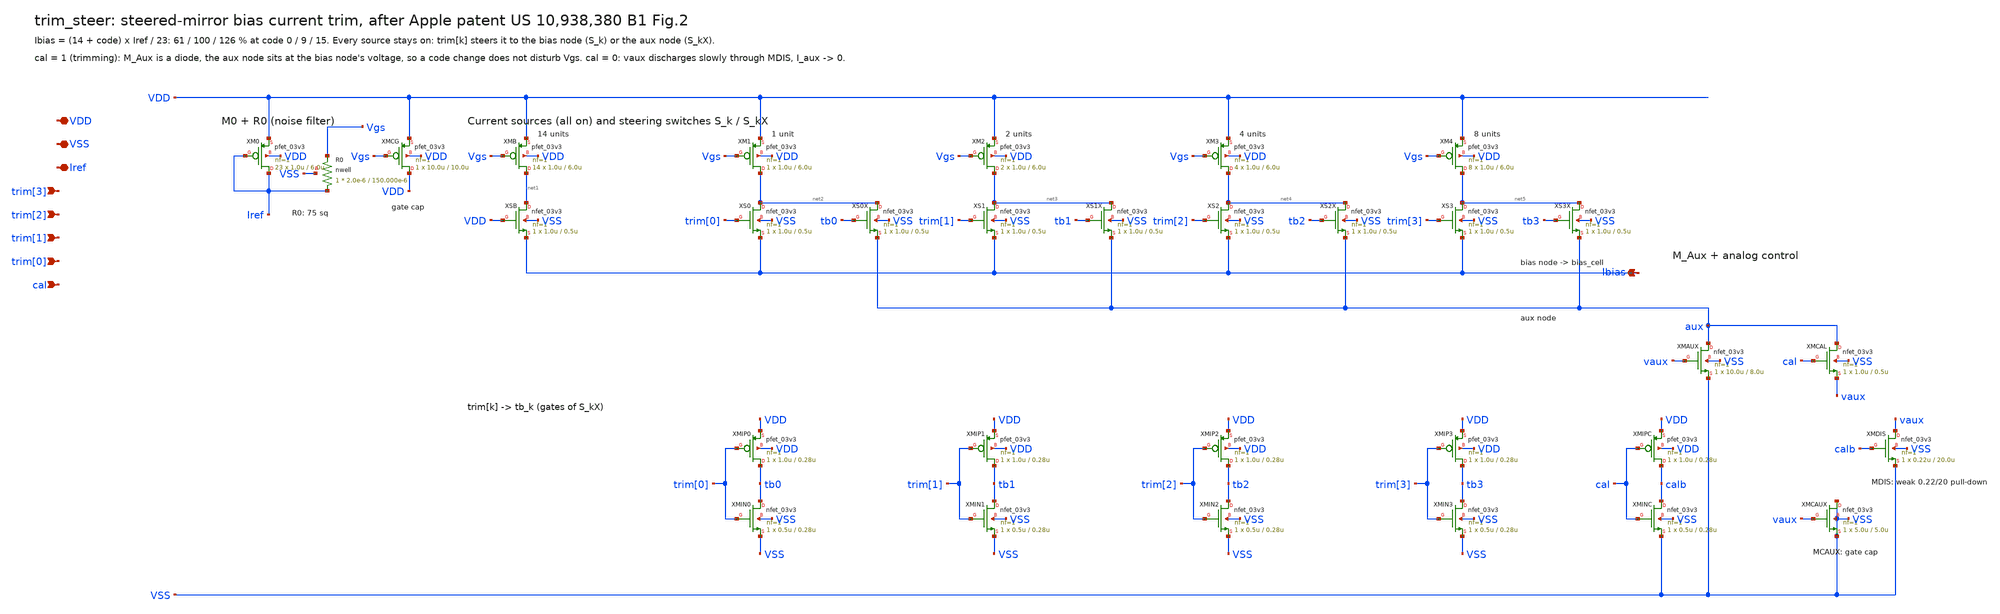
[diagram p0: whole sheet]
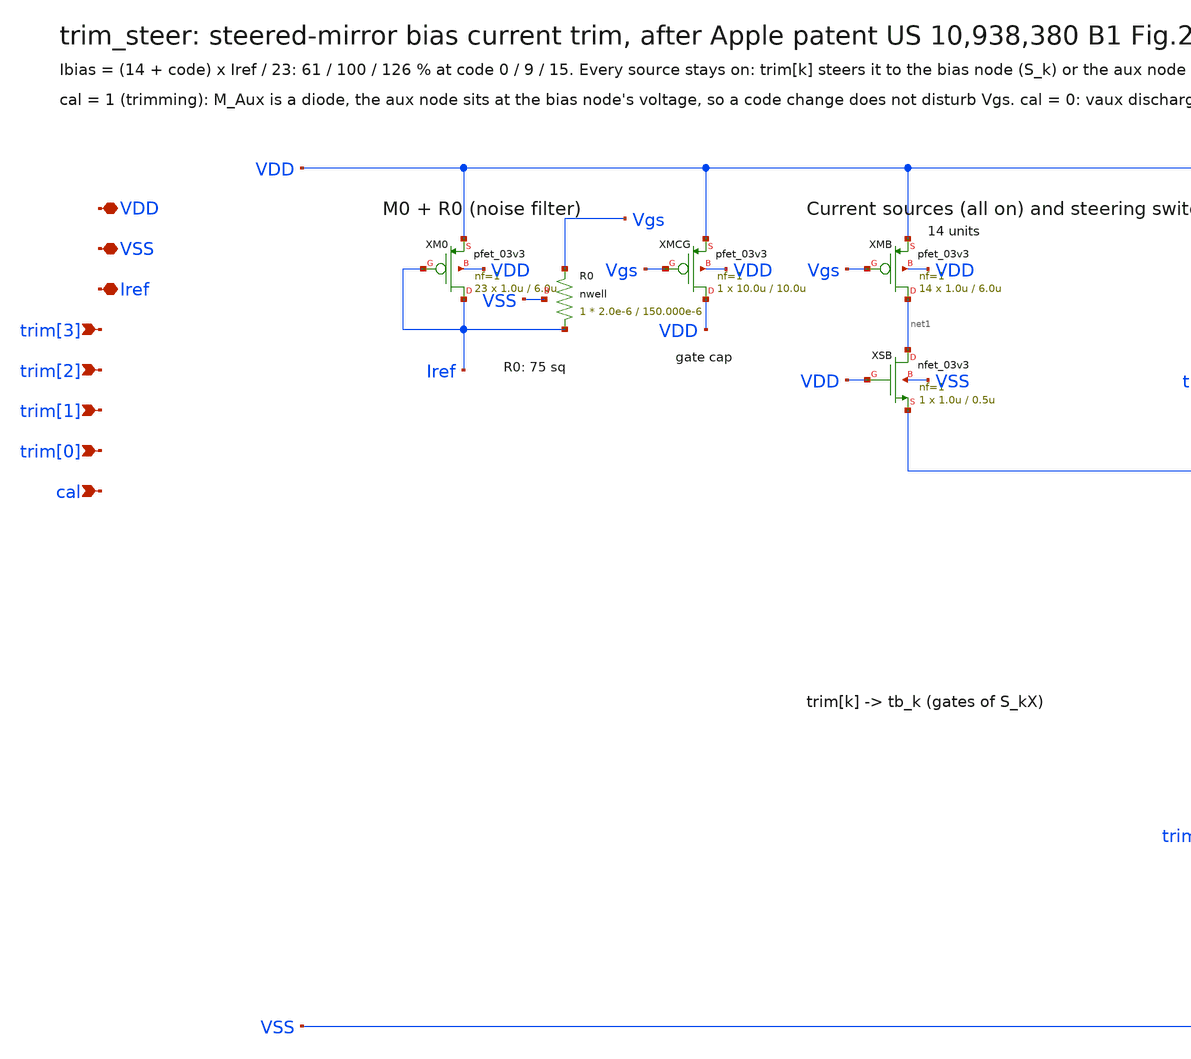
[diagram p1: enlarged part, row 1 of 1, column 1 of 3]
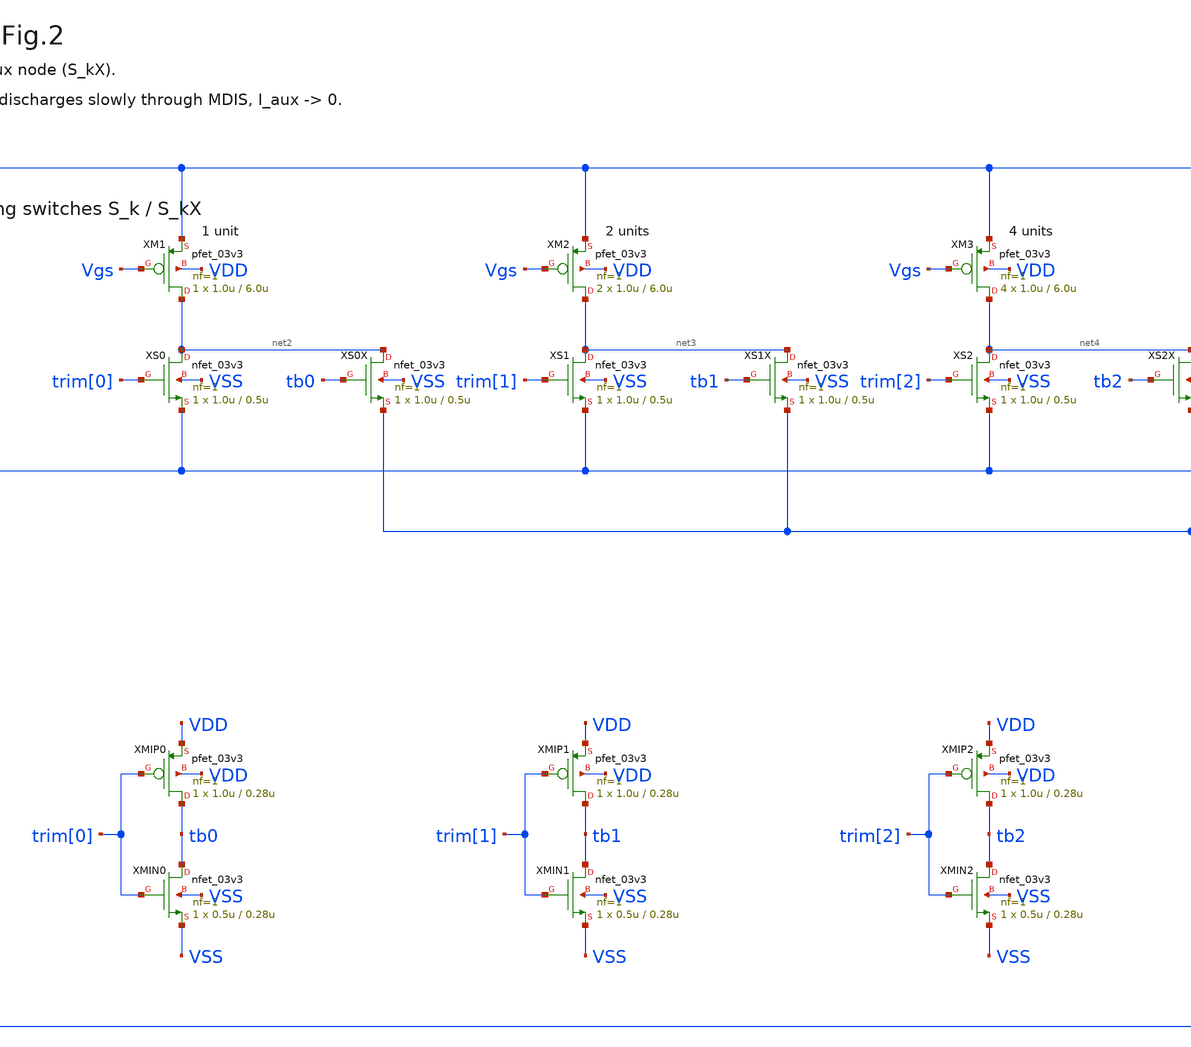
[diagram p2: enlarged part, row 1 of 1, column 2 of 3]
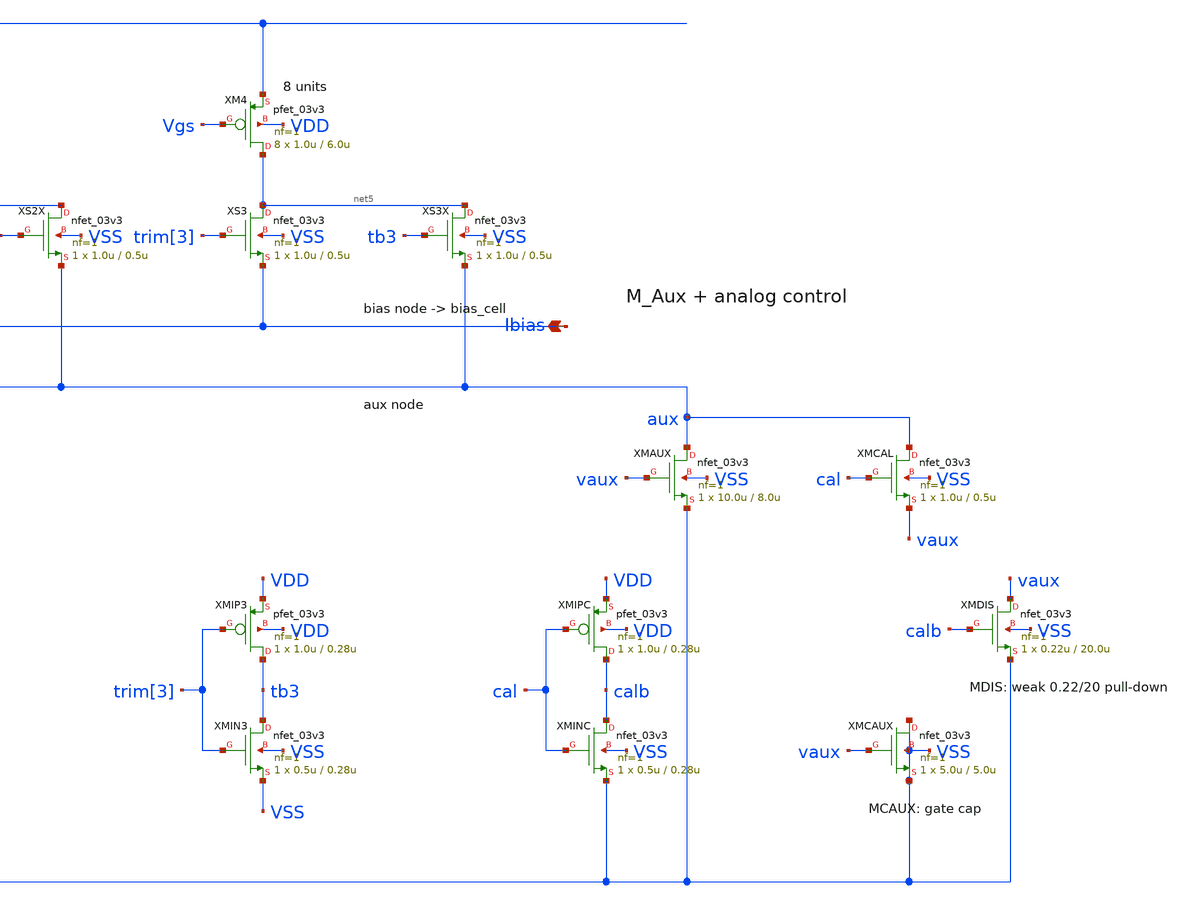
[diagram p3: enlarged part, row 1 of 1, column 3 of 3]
** sch_path: explore/bias/generator/trim_steer.sch
**.subckt trim_steer VDD VSS Iref trim[3] trim[2] trim[1] trim[0] cal Ibias
*.iopin VDD
*.iopin VSS
*.iopin Iref
*.ipin trim[3]
*.ipin trim[2]
*.ipin trim[1]
*.ipin trim[0]
*.ipin cal
*.opin Ibias
XM0 Iref Iref VDD VDD pfet_03v3 L=6.0u W=1.0u nf=1 ad='int((nf+1)/2) * W/nf * 0.18u' as='int((nf+2)/2) * W/nf * 0.18u'
+ pd='2*int((nf+1)/2) * (W/nf + 0.18u)' ps='2*int((nf+2)/2) * (W/nf + 0.18u)' nrd='0.18u / W' nrs='0.18u / W'
+ sa=0 sb=0 sd=0 m=23
XR0 Iref Vgs VSS nwell r_width=2.0e-6 r_length=150.000e-6 m=1
XMCG VDD Vgs VDD VDD pfet_03v3 L=10.0u W=10.0u nf=1 ad='int((nf+1)/2) * W/nf * 0.18u' as='int((nf+2)/2) * W/nf * 0.18u'
+ pd='2*int((nf+1)/2) * (W/nf + 0.18u)' ps='2*int((nf+2)/2) * (W/nf + 0.18u)' nrd='0.18u / W' nrs='0.18u / W'
+ sa=0 sb=0 sd=0 m=1
XMB net1 Vgs VDD VDD pfet_03v3 L=6.0u W=1.0u nf=1 ad='int((nf+1)/2) * W/nf * 0.18u' as='int((nf+2)/2) * W/nf * 0.18u'
+ pd='2*int((nf+1)/2) * (W/nf + 0.18u)' ps='2*int((nf+2)/2) * (W/nf + 0.18u)' nrd='0.18u / W' nrs='0.18u / W'
+ sa=0 sb=0 sd=0 m=14
XSB net1 VDD Ibias VSS nfet_03v3 L=0.5u W=1.0u nf=1 ad='int((nf+1)/2) * W/nf * 0.18u' as='int((nf+2)/2) * W/nf * 0.18u'
+ pd='2*int((nf+1)/2) * (W/nf + 0.18u)' ps='2*int((nf+2)/2) * (W/nf + 0.18u)' nrd='0.18u / W' nrs='0.18u / W'
+ sa=0 sb=0 sd=0 m=1
XM1 net2 Vgs VDD VDD pfet_03v3 L=6.0u W=1.0u nf=1 ad='int((nf+1)/2) * W/nf * 0.18u' as='int((nf+2)/2) * W/nf * 0.18u'
+ pd='2*int((nf+1)/2) * (W/nf + 0.18u)' ps='2*int((nf+2)/2) * (W/nf + 0.18u)' nrd='0.18u / W' nrs='0.18u / W'
+ sa=0 sb=0 sd=0 m=1
XS0 net2 trim[0] Ibias VSS nfet_03v3 L=0.5u W=1.0u nf=1 ad='int((nf+1)/2) * W/nf * 0.18u' as='int((nf+2)/2) * W/nf * 0.18u'
+ pd='2*int((nf+1)/2) * (W/nf + 0.18u)' ps='2*int((nf+2)/2) * (W/nf + 0.18u)' nrd='0.18u / W' nrs='0.18u / W'
+ sa=0 sb=0 sd=0 m=1
XS0X net2 tb0 aux VSS nfet_03v3 L=0.5u W=1.0u nf=1 ad='int((nf+1)/2) * W/nf * 0.18u' as='int((nf+2)/2) * W/nf * 0.18u'
+ pd='2*int((nf+1)/2) * (W/nf + 0.18u)' ps='2*int((nf+2)/2) * (W/nf + 0.18u)' nrd='0.18u / W' nrs='0.18u / W'
+ sa=0 sb=0 sd=0 m=1
XM2 net3 Vgs VDD VDD pfet_03v3 L=6.0u W=1.0u nf=1 ad='int((nf+1)/2) * W/nf * 0.18u' as='int((nf+2)/2) * W/nf * 0.18u'
+ pd='2*int((nf+1)/2) * (W/nf + 0.18u)' ps='2*int((nf+2)/2) * (W/nf + 0.18u)' nrd='0.18u / W' nrs='0.18u / W'
+ sa=0 sb=0 sd=0 m=2
XS1 net3 trim[1] Ibias VSS nfet_03v3 L=0.5u W=1.0u nf=1 ad='int((nf+1)/2) * W/nf * 0.18u' as='int((nf+2)/2) * W/nf * 0.18u'
+ pd='2*int((nf+1)/2) * (W/nf + 0.18u)' ps='2*int((nf+2)/2) * (W/nf + 0.18u)' nrd='0.18u / W' nrs='0.18u / W'
+ sa=0 sb=0 sd=0 m=1
XS1X net3 tb1 aux VSS nfet_03v3 L=0.5u W=1.0u nf=1 ad='int((nf+1)/2) * W/nf * 0.18u' as='int((nf+2)/2) * W/nf * 0.18u'
+ pd='2*int((nf+1)/2) * (W/nf + 0.18u)' ps='2*int((nf+2)/2) * (W/nf + 0.18u)' nrd='0.18u / W' nrs='0.18u / W'
+ sa=0 sb=0 sd=0 m=1
XM3 net4 Vgs VDD VDD pfet_03v3 L=6.0u W=1.0u nf=1 ad='int((nf+1)/2) * W/nf * 0.18u' as='int((nf+2)/2) * W/nf * 0.18u'
+ pd='2*int((nf+1)/2) * (W/nf + 0.18u)' ps='2*int((nf+2)/2) * (W/nf + 0.18u)' nrd='0.18u / W' nrs='0.18u / W'
+ sa=0 sb=0 sd=0 m=4
XS2 net4 trim[2] Ibias VSS nfet_03v3 L=0.5u W=1.0u nf=1 ad='int((nf+1)/2) * W/nf * 0.18u' as='int((nf+2)/2) * W/nf * 0.18u'
+ pd='2*int((nf+1)/2) * (W/nf + 0.18u)' ps='2*int((nf+2)/2) * (W/nf + 0.18u)' nrd='0.18u / W' nrs='0.18u / W'
+ sa=0 sb=0 sd=0 m=1
XS2X net4 tb2 aux VSS nfet_03v3 L=0.5u W=1.0u nf=1 ad='int((nf+1)/2) * W/nf * 0.18u' as='int((nf+2)/2) * W/nf * 0.18u'
+ pd='2*int((nf+1)/2) * (W/nf + 0.18u)' ps='2*int((nf+2)/2) * (W/nf + 0.18u)' nrd='0.18u / W' nrs='0.18u / W'
+ sa=0 sb=0 sd=0 m=1
XM4 net5 Vgs VDD VDD pfet_03v3 L=6.0u W=1.0u nf=1 ad='int((nf+1)/2) * W/nf * 0.18u' as='int((nf+2)/2) * W/nf * 0.18u'
+ pd='2*int((nf+1)/2) * (W/nf + 0.18u)' ps='2*int((nf+2)/2) * (W/nf + 0.18u)' nrd='0.18u / W' nrs='0.18u / W'
+ sa=0 sb=0 sd=0 m=8
XS3 net5 trim[3] Ibias VSS nfet_03v3 L=0.5u W=1.0u nf=1 ad='int((nf+1)/2) * W/nf * 0.18u' as='int((nf+2)/2) * W/nf * 0.18u'
+ pd='2*int((nf+1)/2) * (W/nf + 0.18u)' ps='2*int((nf+2)/2) * (W/nf + 0.18u)' nrd='0.18u / W' nrs='0.18u / W'
+ sa=0 sb=0 sd=0 m=1
XS3X net5 tb3 aux VSS nfet_03v3 L=0.5u W=1.0u nf=1 ad='int((nf+1)/2) * W/nf * 0.18u' as='int((nf+2)/2) * W/nf * 0.18u'
+ pd='2*int((nf+1)/2) * (W/nf + 0.18u)' ps='2*int((nf+2)/2) * (W/nf + 0.18u)' nrd='0.18u / W' nrs='0.18u / W'
+ sa=0 sb=0 sd=0 m=1
XMIP0 tb0 trim[0] VDD VDD pfet_03v3 L=0.28u W=1.0u nf=1 ad='int((nf+1)/2) * W/nf * 0.18u' as='int((nf+2)/2) * W/nf * 0.18u'
+ pd='2*int((nf+1)/2) * (W/nf + 0.18u)' ps='2*int((nf+2)/2) * (W/nf + 0.18u)' nrd='0.18u / W' nrs='0.18u / W'
+ sa=0 sb=0 sd=0 m=1
XMIN0 tb0 trim[0] VSS VSS nfet_03v3 L=0.28u W=0.5u nf=1 ad='int((nf+1)/2) * W/nf * 0.18u' as='int((nf+2)/2) * W/nf * 0.18u'
+ pd='2*int((nf+1)/2) * (W/nf + 0.18u)' ps='2*int((nf+2)/2) * (W/nf + 0.18u)' nrd='0.18u / W' nrs='0.18u / W'
+ sa=0 sb=0 sd=0 m=1
XMIP1 tb1 trim[1] VDD VDD pfet_03v3 L=0.28u W=1.0u nf=1 ad='int((nf+1)/2) * W/nf * 0.18u' as='int((nf+2)/2) * W/nf * 0.18u'
+ pd='2*int((nf+1)/2) * (W/nf + 0.18u)' ps='2*int((nf+2)/2) * (W/nf + 0.18u)' nrd='0.18u / W' nrs='0.18u / W'
+ sa=0 sb=0 sd=0 m=1
XMIN1 tb1 trim[1] VSS VSS nfet_03v3 L=0.28u W=0.5u nf=1 ad='int((nf+1)/2) * W/nf * 0.18u' as='int((nf+2)/2) * W/nf * 0.18u'
+ pd='2*int((nf+1)/2) * (W/nf + 0.18u)' ps='2*int((nf+2)/2) * (W/nf + 0.18u)' nrd='0.18u / W' nrs='0.18u / W'
+ sa=0 sb=0 sd=0 m=1
XMIP2 tb2 trim[2] VDD VDD pfet_03v3 L=0.28u W=1.0u nf=1 ad='int((nf+1)/2) * W/nf * 0.18u' as='int((nf+2)/2) * W/nf * 0.18u'
+ pd='2*int((nf+1)/2) * (W/nf + 0.18u)' ps='2*int((nf+2)/2) * (W/nf + 0.18u)' nrd='0.18u / W' nrs='0.18u / W'
+ sa=0 sb=0 sd=0 m=1
XMIN2 tb2 trim[2] VSS VSS nfet_03v3 L=0.28u W=0.5u nf=1 ad='int((nf+1)/2) * W/nf * 0.18u' as='int((nf+2)/2) * W/nf * 0.18u'
+ pd='2*int((nf+1)/2) * (W/nf + 0.18u)' ps='2*int((nf+2)/2) * (W/nf + 0.18u)' nrd='0.18u / W' nrs='0.18u / W'
+ sa=0 sb=0 sd=0 m=1
XMIP3 tb3 trim[3] VDD VDD pfet_03v3 L=0.28u W=1.0u nf=1 ad='int((nf+1)/2) * W/nf * 0.18u' as='int((nf+2)/2) * W/nf * 0.18u'
+ pd='2*int((nf+1)/2) * (W/nf + 0.18u)' ps='2*int((nf+2)/2) * (W/nf + 0.18u)' nrd='0.18u / W' nrs='0.18u / W'
+ sa=0 sb=0 sd=0 m=1
XMIN3 tb3 trim[3] VSS VSS nfet_03v3 L=0.28u W=0.5u nf=1 ad='int((nf+1)/2) * W/nf * 0.18u' as='int((nf+2)/2) * W/nf * 0.18u'
+ pd='2*int((nf+1)/2) * (W/nf + 0.18u)' ps='2*int((nf+2)/2) * (W/nf + 0.18u)' nrd='0.18u / W' nrs='0.18u / W'
+ sa=0 sb=0 sd=0 m=1
XMAUX aux vaux VSS VSS nfet_03v3 L=8.0u W=10.0u nf=1 ad='int((nf+1)/2) * W/nf * 0.18u' as='int((nf+2)/2) * W/nf * 0.18u'
+ pd='2*int((nf+1)/2) * (W/nf + 0.18u)' ps='2*int((nf+2)/2) * (W/nf + 0.18u)' nrd='0.18u / W' nrs='0.18u / W'
+ sa=0 sb=0 sd=0 m=1
XMCAL aux cal vaux VSS nfet_03v3 L=0.5u W=1.0u nf=1 ad='int((nf+1)/2) * W/nf * 0.18u' as='int((nf+2)/2) * W/nf * 0.18u'
+ pd='2*int((nf+1)/2) * (W/nf + 0.18u)' ps='2*int((nf+2)/2) * (W/nf + 0.18u)' nrd='0.18u / W' nrs='0.18u / W'
+ sa=0 sb=0 sd=0 m=1
XMDIS vaux calb VSS VSS nfet_03v3 L=20.0u W=0.22u nf=1 ad='int((nf+1)/2) * W/nf * 0.18u' as='int((nf+2)/2) * W/nf * 0.18u'
+ pd='2*int((nf+1)/2) * (W/nf + 0.18u)' ps='2*int((nf+2)/2) * (W/nf + 0.18u)' nrd='0.18u / W' nrs='0.18u / W'
+ sa=0 sb=0 sd=0 m=1
XMCAUX VSS vaux VSS VSS nfet_03v3 L=5.0u W=5.0u nf=1 ad='int((nf+1)/2) * W/nf * 0.18u' as='int((nf+2)/2) * W/nf * 0.18u'
+ pd='2*int((nf+1)/2) * (W/nf + 0.18u)' ps='2*int((nf+2)/2) * (W/nf + 0.18u)' nrd='0.18u / W' nrs='0.18u / W'
+ sa=0 sb=0 sd=0 m=1
XMIPC calb cal VDD VDD pfet_03v3 L=0.28u W=1.0u nf=1 ad='int((nf+1)/2) * W/nf * 0.18u' as='int((nf+2)/2) * W/nf * 0.18u'
+ pd='2*int((nf+1)/2) * (W/nf + 0.18u)' ps='2*int((nf+2)/2) * (W/nf + 0.18u)' nrd='0.18u / W' nrs='0.18u / W'
+ sa=0 sb=0 sd=0 m=1
XMINC calb cal VSS VSS nfet_03v3 L=0.28u W=0.5u nf=1 ad='int((nf+1)/2) * W/nf * 0.18u' as='int((nf+2)/2) * W/nf * 0.18u'
+ pd='2*int((nf+1)/2) * (W/nf + 0.18u)' ps='2*int((nf+2)/2) * (W/nf + 0.18u)' nrd='0.18u / W' nrs='0.18u / W'
+ sa=0 sb=0 sd=0 m=1
**.ends
.end
